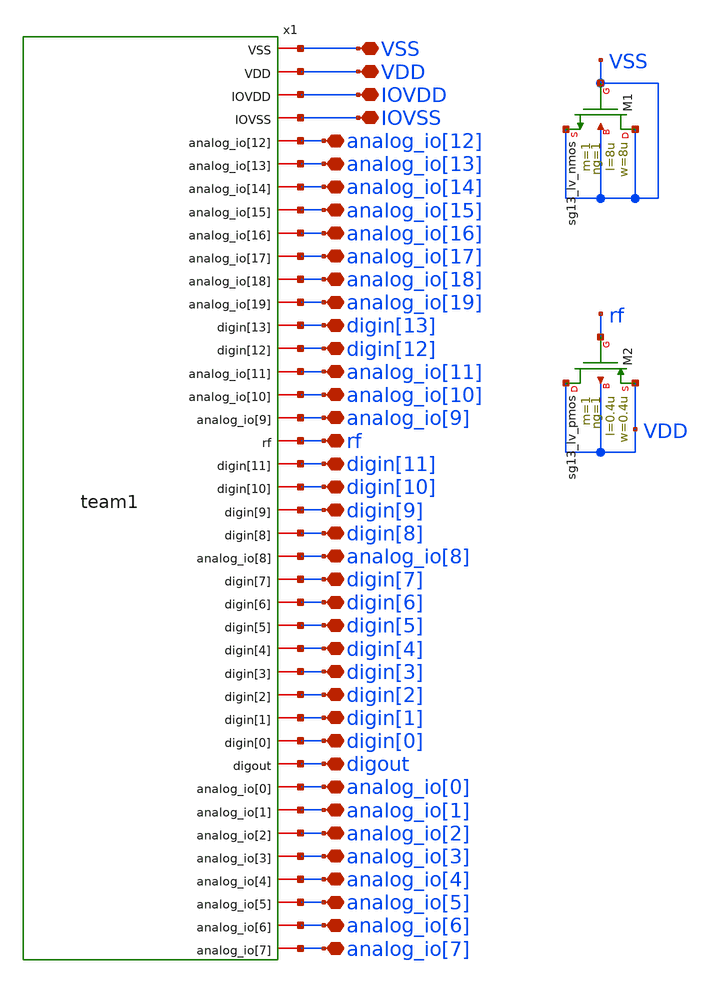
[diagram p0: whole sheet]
** sch_path: UNIC-CASS-2025/final-chip/xschem/MPC0388.sch
**.subckt MPC0388 VSS VDD IOVDD IOVSS digout rf analog_io[19] analog_io[18] analog_io[17]
*+ analog_io[16] analog_io[14] analog_io[13] analog_io[12] analog_io[11] analog_io[10] analog_io[9] analog_io[7]
*+ analog_io[6] analog_io[5] analog_io[4] analog_io[3] analog_io[2] analog_io[1] analog_io[8] analog_io[0]
*+ digin[13] digin[12] digin[11] digin[10] digin[9] digin[8] digin[7] digin[6] digin[5] digin[4] digin[3]
*+ digin[2] digin[1] digin[0] analog_io[15]
*.iopin VSS
*.iopin VDD
*.iopin IOVDD
*.iopin IOVSS
*.iopin digout
*.iopin rf
*.iopin analog_io[19]
*.iopin analog_io[18]
*.iopin analog_io[17]
*.iopin analog_io[16]
*.iopin analog_io[14]
*.iopin analog_io[13]
*.iopin analog_io[12]
*.iopin analog_io[11]
*.iopin analog_io[10]
*.iopin analog_io[9]
*.iopin analog_io[7]
*.iopin analog_io[6]
*.iopin analog_io[5]
*.iopin analog_io[4]
*.iopin analog_io[3]
*.iopin analog_io[2]
*.iopin analog_io[1]
*.iopin analog_io[8]
*.iopin analog_io[0]
*.iopin digin[13]
*.iopin digin[12]
*.iopin digin[11]
*.iopin digin[10]
*.iopin digin[9]
*.iopin digin[8]
*.iopin digin[7]
*.iopin digin[6]
*.iopin digin[5]
*.iopin digin[4]
*.iopin digin[3]
*.iopin digin[2]
*.iopin digin[1]
*.iopin digin[0]
*.iopin analog_io[15]
x1 VSS VDD IOVDD IOVSS analog_io[12] analog_io[13] analog_io[14] analog_io[15] analog_io[16]
+ analog_io[17] analog_io[18] analog_io[19] digin[13] digin[12] analog_io[11] analog_io[10] analog_io[9] rf
+ digin[11] digin[10] digin[9] digin[8] analog_io[8] digin[7] digin[6] digin[5] digin[4] digin[3] digin[2]
+ digin[1] digin[0] digout analog_io[0] analog_io[1] analog_io[2] analog_io[3] analog_io[4] analog_io[5]
+ analog_io[6] analog_io[7] team1
XM1 VSS VSS VSS VSS sg13_lv_nmos w=8u l=8u ng=1 m=1 mm_ok=1
XM2 VDD rf VDD VDD sg13_lv_pmos w=0.4u l=0.4u ng=1 m=1 mm_ok=1
**.ends
.end
